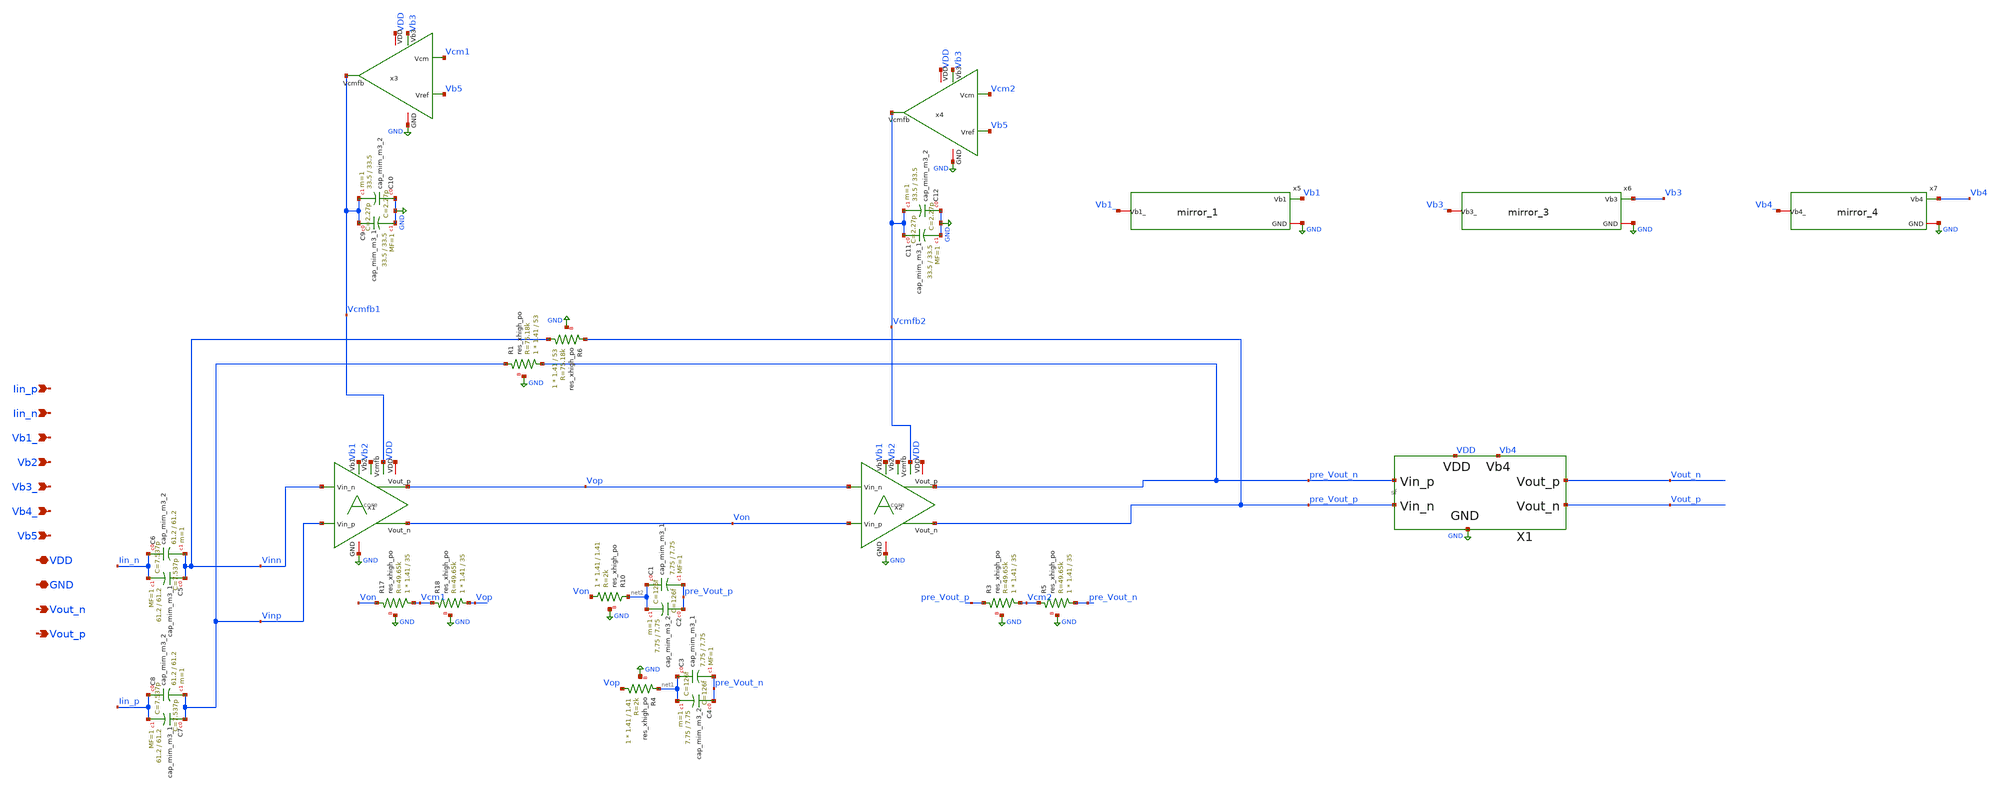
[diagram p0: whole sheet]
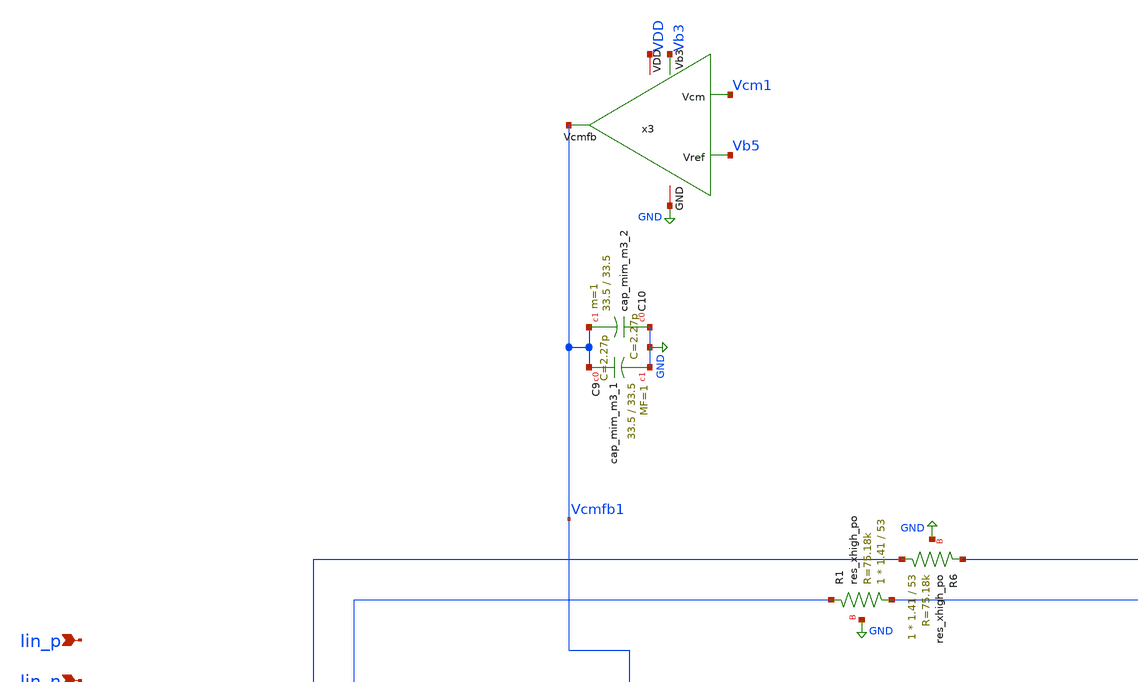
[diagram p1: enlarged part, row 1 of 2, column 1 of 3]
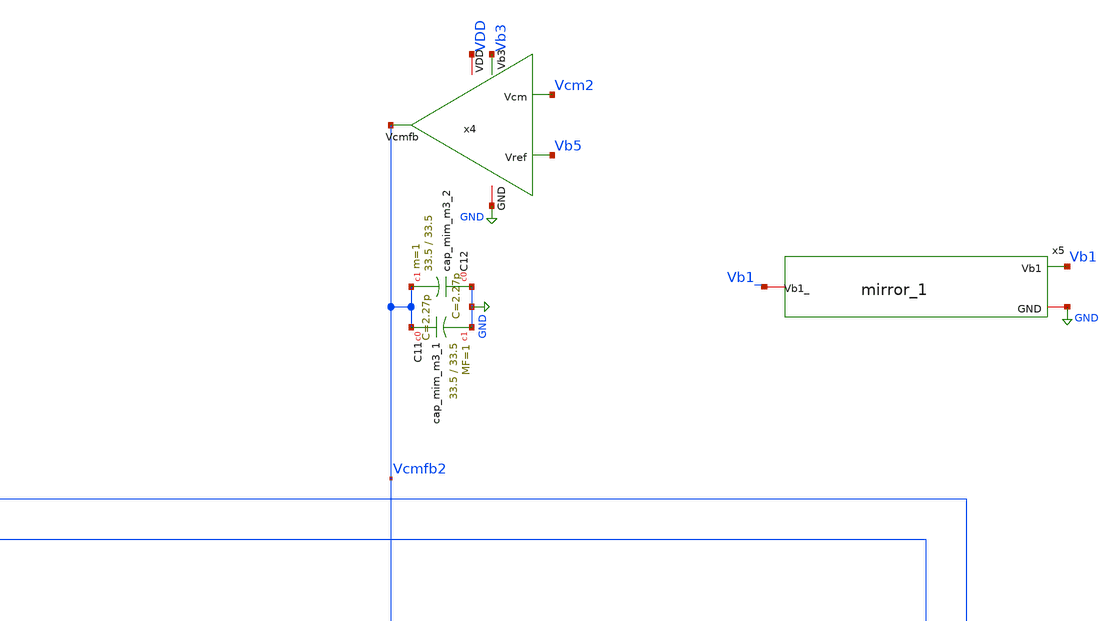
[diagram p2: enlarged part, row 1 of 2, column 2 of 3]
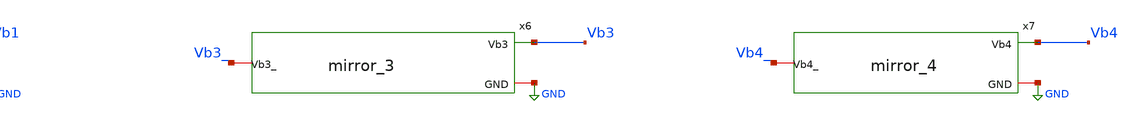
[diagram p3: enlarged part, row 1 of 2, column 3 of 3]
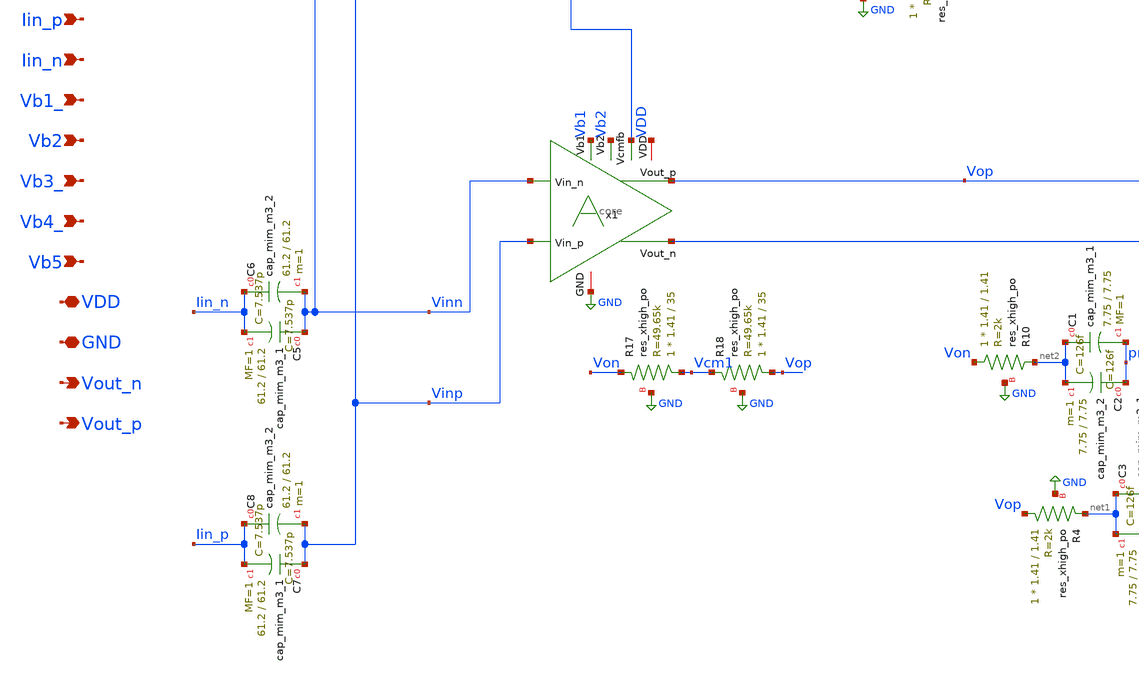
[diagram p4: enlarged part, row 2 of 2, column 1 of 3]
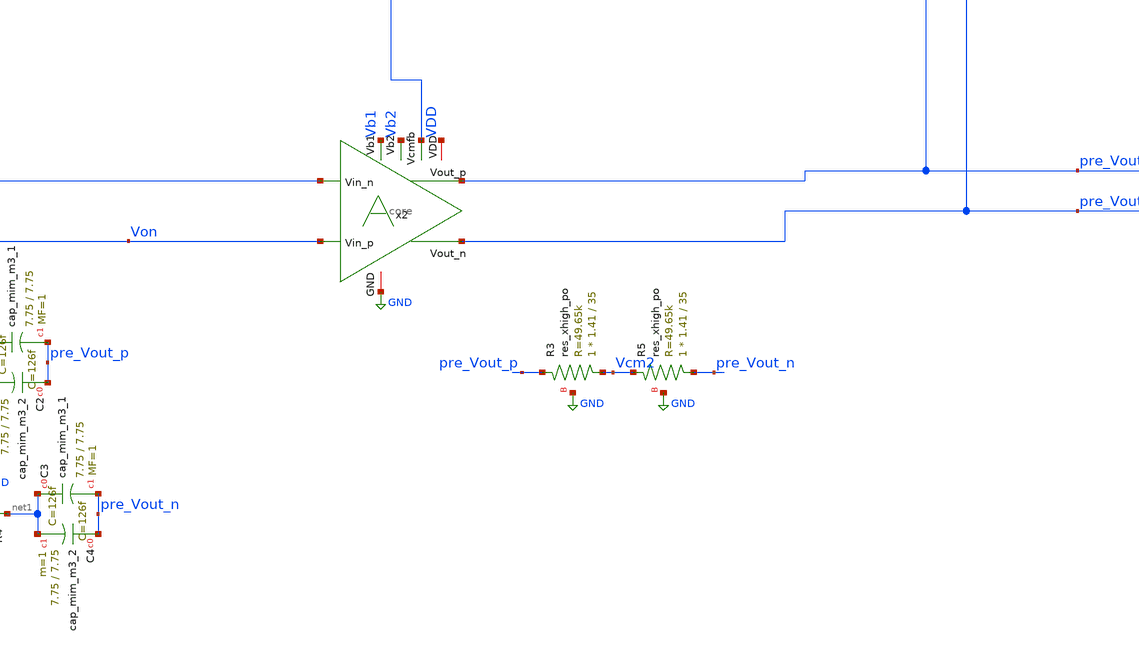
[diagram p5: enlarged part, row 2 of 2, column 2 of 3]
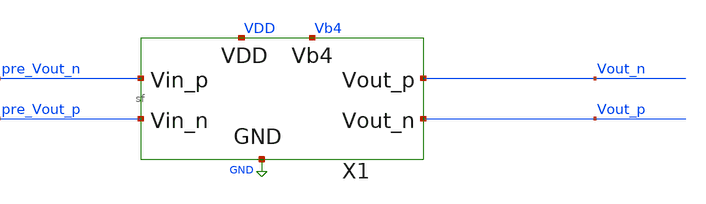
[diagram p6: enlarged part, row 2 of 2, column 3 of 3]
** sch_path: xschem/top.sch
**.subckt top VDD GND Vout_n Iin_n Iin_p Vb1_ Vout_p Vb2 Vb3_ Vb4_ Vb5
*.iopin VDD
*.iopin GND
*.opin Vout_n
*.ipin Iin_n
*.ipin Iin_p
*.ipin Vb1_
*.opin Vout_p
*.ipin Vb2
*.ipin Vb3_
*.ipin Vb4_
*.ipin Vb5
XR6 Vinn pre_Vout_p GND sky130_fd_pr__res_xhigh_po W=1.41 L=53 mult=1 m=1
XR1 pre_Vout_n Vinp GND sky130_fd_pr__res_xhigh_po W=1.41 L=53 mult=1 m=1
XR3 Vcm2 pre_Vout_p GND sky130_fd_pr__res_xhigh_po W=1.41 L=35 mult=1 m=1
XR5 pre_Vout_n Vcm2 GND sky130_fd_pr__res_xhigh_po W=1.41 L=35 mult=1 m=1
XR4 Vop net1 GND sky130_fd_pr__res_xhigh_po W=1.41 L=1.41 mult=1 m=1
XR10 Von net2 GND sky130_fd_pr__res_xhigh_po W=1.41 L=1.41 mult=1 m=1
XR17 Vcm1 Von GND sky130_fd_pr__res_xhigh_po W=1.41 L=35 mult=1 m=1
XR18 Vop Vcm1 GND sky130_fd_pr__res_xhigh_po W=1.41 L=35 mult=1 m=1
x1 Vinn Vinp Vb2 Vb1 Vcmfb1 VDD GND Vop Von core
x2 Vop Von Vb2 Vb1 Vcmfb2 VDD GND pre_Vout_n pre_Vout_p core
X1 VDD GND pre_Vout_n pre_Vout_p Vout_n Vout_p Vb4 sf
x3 Vcm1 Vb5 Vb3 VDD GND Vcmfb1 cmfb
x4 Vcm2 Vb5 Vb3 VDD GND Vcmfb2 cmfb
x5 Vb1 Vb1_ GND mirror_1
x6 Vb3 Vb3_ GND mirror_3
x7 Vb4 Vb4_ GND mirror_4
XC3 net1 pre_Vout_n sky130_fd_pr__cap_mim_m3_1 W=7.75 L=7.75 MF=1 m=1
XC4 pre_Vout_n net1 sky130_fd_pr__cap_mim_m3_2 W=7.75 L=7.75 MF=1 m=1
XC1 net2 pre_Vout_p sky130_fd_pr__cap_mim_m3_1 W=7.75 L=7.75 MF=1 m=1
XC2 pre_Vout_p net2 sky130_fd_pr__cap_mim_m3_2 W=7.75 L=7.75 MF=1 m=1
XC5 Vinn Iin_n sky130_fd_pr__cap_mim_m3_1 W=61.2 L=61.2 MF=1 m=1
XC6 Iin_n Vinn sky130_fd_pr__cap_mim_m3_2 W=61.2 L=61.2 MF=1 m=1
XC7 Vinp Iin_p sky130_fd_pr__cap_mim_m3_1 W=61.2 L=61.2 MF=1 m=1
XC8 Iin_p Vinp sky130_fd_pr__cap_mim_m3_2 W=61.2 L=61.2 MF=1 m=1
XC9 Vcmfb1 GND sky130_fd_pr__cap_mim_m3_1 W=33.5 L=33.5 MF=1 m=1
XC10 GND Vcmfb1 sky130_fd_pr__cap_mim_m3_2 W=33.5 L=33.5 MF=1 m=1
XC11 Vcmfb2 GND sky130_fd_pr__cap_mim_m3_1 W=33.5 L=33.5 MF=1 m=1
XC12 GND Vcmfb2 sky130_fd_pr__cap_mim_m3_2 W=33.5 L=33.5 MF=1 m=1
**.ends

* expanding   symbol:  tia_post_approval/schem/core.sym # of pins=9
** sym_path: tia_post_approval/schem/core.sym
** sch_path: tia_post_approval/schem/core.sch
.subckt core Vin_n Vin_p Vb2 Vb1 Vcmfb VDD GND Vout_p Vout_n
*.ipin Vb2
*.ipin Vcmfb
*.iopin VDD
*.iopin GND
*.opin Vout_p
*.ipin Vin_p
*.ipin Vin_n
*.opin Vout_n
*.ipin Vb1
XM1 net1 Vb1 GND GND sky130_fd_pr__nfet_01v8 L=.5 W=710 nf=8 ad='int((nf+1)/2) * W/nf * 0.29' as='int((nf+2)/2) * W/nf * 0.29'
+ pd='2*int((nf+1)/2) * (W/nf + 0.29)' ps='2*int((nf+2)/2) * (W/nf + 0.29)' nrd='0.29 / W' nrs='0.29 / W'
+ sa=0 sb=0 sd=0 mult=1 m=1
x1 Vin_p Vb2 Vcmfb VDD GND Vout_n net1 core_half
x2 Vin_n Vb2 Vcmfb VDD GND Vout_p net1 core_half
.ends


* expanding   symbol:  tia_post_approval/schem/sf.sym # of pins=7
** sym_path: tia_post_approval/schem/sf.sym
** sch_path: tia_post_approval/schem/sf.sch
.subckt sf VDD GND Vin_p Vin_n Vout_p Vout_n Vb4
*.ipin Vin_n
*.iopin VDD
*.iopin GND
*.ipin Vin_p
*.opin Vout_n
*.opin Vout_p
*.iopin Vb4
X1 VDD Vb4 Vout_p Vin_p GND sf_half
X2 VDD Vb4 Vout_n Vin_n GND sf_half
.ends


* expanding   symbol:  tia_post_approval/schem/cmfb.sym # of pins=6
** sym_path: tia_post_approval/schem/cmfb.sym
** sch_path: tia_post_approval/schem/cmfb.sch
.subckt cmfb Vcm Vref Vb3 VDD GND Vcmfb
*.iopin VDD
*.iopin GND
*.opin Vcmfb
*.ipin Vref
*.iopin Vb3
*.ipin Vcm
x1 Vref net2 VDD GND Vb3 net3 Vcmfb cmfb_half
x2 Vcm net1 VDD GND Vb3 net3 net3 cmfb_half
XR20 net2 net1 GND sky130_fd_pr__res_xhigh_po W=1.41 L=1.41 mult=1 m=1
.ends


* expanding   symbol:  tia_post_approval/schem/mirror_1.sym # of pins=3
** sym_path: tia_post_approval/schem/mirror_1.sym
** sch_path: tia_post_approval/schem/mirror_1.sch
.subckt mirror_1 Vb1 Vb1_ GND
*.iopin GND
*.iopin Vb1_
*.opin Vb1
XM27 Vb1_ Vb1_ GND GND sky130_fd_pr__nfet_01v8 L=.5 W=3.6 nf=1 ad='int((nf+1)/2) * W/nf * 0.29' as='int((nf+2)/2) * W/nf * 0.29'
+ pd='2*int((nf+1)/2) * (W/nf + 0.29)' ps='2*int((nf+2)/2) * (W/nf + 0.29)' nrd='0.29 / W' nrs='0.29 / W'
+ sa=0 sb=0 sd=0 mult=1 m=1
XC1 Vb1 GND sky130_fd_pr__cap_mim_m3_1 W=15.8 L=15.8 MF=1 m=1
XC2 GND Vb1 sky130_fd_pr__cap_mim_m3_2 W=15.8 L=15.8 MF=1 m=1
XR11 V10 Vb1 GND sky130_fd_pr__res_xhigh_po W=0.35 L=16 mult=1 m=1
XR1 Vb1_ V1 GND sky130_fd_pr__res_xhigh_po W=0.35 L=16 mult=1 m=1
XR2 V10 V9 GND sky130_fd_pr__res_xhigh_po W=0.35 L=16 mult=1 m=1
XR3 V2 V1 GND sky130_fd_pr__res_xhigh_po W=0.35 L=16 mult=1 m=1
XR4 V8 V9 GND sky130_fd_pr__res_xhigh_po W=0.35 L=16 mult=1 m=1
XR5 V2 V3 GND sky130_fd_pr__res_xhigh_po W=0.35 L=16 mult=1 m=1
XR6 V8 V7 GND sky130_fd_pr__res_xhigh_po W=0.35 L=16 mult=1 m=1
XR7 V4 V3 GND sky130_fd_pr__res_xhigh_po W=0.35 L=16 mult=1 m=1
XR8 V6 V7 GND sky130_fd_pr__res_xhigh_po W=0.35 L=16 mult=1 m=1
XR9 V4 V5 GND sky130_fd_pr__res_xhigh_po W=0.35 L=16 mult=1 m=1
XR10 V6 V5 GND sky130_fd_pr__res_xhigh_po W=0.35 L=16 mult=1 m=1
XM1 GND GND Vb1_ GND sky130_fd_pr__nfet_01v8 L=.5 W=3.6 nf=1 ad='int((nf+1)/2) * W/nf * 0.29' as='int((nf+2)/2) * W/nf * 0.29'
+ pd='2*int((nf+1)/2) * (W/nf + 0.29)' ps='2*int((nf+2)/2) * (W/nf + 0.29)' nrd='0.29 / W' nrs='0.29 / W'
+ sa=0 sb=0 sd=0 mult=1 m=1
XM2 GND GND GND GND sky130_fd_pr__nfet_01v8 L=.5 W=3.6 nf=1 ad='int((nf+1)/2) * W/nf * 0.29' as='int((nf+2)/2) * W/nf * 0.29'
+ pd='2*int((nf+1)/2) * (W/nf + 0.29)' ps='2*int((nf+2)/2) * (W/nf + 0.29)' nrd='0.29 / W' nrs='0.29 / W'
+ sa=0 sb=0 sd=0 mult=1 m=1
.ends


* expanding   symbol:  tia_post_approval/schem/mirror_3.sym # of pins=3
** sym_path: tia_post_approval/schem/mirror_3.sym
** sch_path: tia_post_approval/schem/mirror_3.sch
.subckt mirror_3 Vb3 Vb3_ GND
*.iopin GND
*.iopin Vb3_
*.opin Vb3
XM27 Vb3_ Vb3_ GND GND sky130_fd_pr__nfet_01v8 L=.5 W=5 nf=1 ad='int((nf+1)/2) * W/nf * 0.29' as='int((nf+2)/2) * W/nf * 0.29'
+ pd='2*int((nf+1)/2) * (W/nf + 0.29)' ps='2*int((nf+2)/2) * (W/nf + 0.29)' nrd='0.29 / W' nrs='0.29 / W'
+ sa=0 sb=0 sd=0 mult=2 m=2
XR11 V10 Vb3 GND sky130_fd_pr__res_xhigh_po W=0.35 L=16 mult=1 m=1
XC1 Vb3 GND sky130_fd_pr__cap_mim_m3_1 W=15.8 L=15.8 MF=1 m=1
XC2 GND Vb3 sky130_fd_pr__cap_mim_m3_2 W=15.8 L=15.8 MF=1 m=1
XR1 Vb3_ V1 GND sky130_fd_pr__res_xhigh_po W=0.35 L=16 mult=1 m=1
XR2 V10 V9 GND sky130_fd_pr__res_xhigh_po W=0.35 L=16 mult=1 m=1
XR3 V2 V1 GND sky130_fd_pr__res_xhigh_po W=0.35 L=16 mult=1 m=1
XR4 V8 V9 GND sky130_fd_pr__res_xhigh_po W=0.35 L=16 mult=1 m=1
XR5 V2 V3 GND sky130_fd_pr__res_xhigh_po W=0.35 L=16 mult=1 m=1
XR6 V8 V7 GND sky130_fd_pr__res_xhigh_po W=0.35 L=16 mult=1 m=1
XR7 V4 V3 GND sky130_fd_pr__res_xhigh_po W=0.35 L=16 mult=1 m=1
XR8 V6 V7 GND sky130_fd_pr__res_xhigh_po W=0.35 L=16 mult=1 m=1
XR9 V4 V5 GND sky130_fd_pr__res_xhigh_po W=0.35 L=16 mult=1 m=1
XR10 V6 V5 GND sky130_fd_pr__res_xhigh_po W=0.35 L=16 mult=1 m=1
.ends


* expanding   symbol:  tia_post_approval/schem/mirror_4.sym # of pins=3
** sym_path: tia_post_approval/schem/mirror_4.sym
** sch_path: tia_post_approval/schem/mirror_4.sch
.subckt mirror_4 Vb4 Vb4_ GND
*.iopin GND
*.iopin Vb4_
*.opin Vb4
XM27 Vb4_ Vb4_ GND GND sky130_fd_pr__nfet_01v8 L=.45 W=4 nf=1 ad='int((nf+1)/2) * W/nf * 0.29' as='int((nf+2)/2) * W/nf * 0.29'
+ pd='2*int((nf+1)/2) * (W/nf + 0.29)' ps='2*int((nf+2)/2) * (W/nf + 0.29)' nrd='0.29 / W' nrs='0.29 / W'
+ sa=0 sb=0 sd=0 mult=1 m=1
XC1 Vb4 GND sky130_fd_pr__cap_mim_m3_1 W=15.8 L=15.8 MF=1 m=1
XC2 GND Vb4 sky130_fd_pr__cap_mim_m3_2 W=15.8 L=15.8 MF=1 m=1
XR11 V10 Vb4 GND sky130_fd_pr__res_xhigh_po W=0.35 L=16 mult=1 m=1
XR1 Vb4_ V1 GND sky130_fd_pr__res_xhigh_po W=0.35 L=16 mult=1 m=1
XR2 V10 V9 GND sky130_fd_pr__res_xhigh_po W=0.35 L=16 mult=1 m=1
XR3 V2 V1 GND sky130_fd_pr__res_xhigh_po W=0.35 L=16 mult=1 m=1
XR4 V8 V9 GND sky130_fd_pr__res_xhigh_po W=0.35 L=16 mult=1 m=1
XR5 V2 V3 GND sky130_fd_pr__res_xhigh_po W=0.35 L=16 mult=1 m=1
XR6 V8 V7 GND sky130_fd_pr__res_xhigh_po W=0.35 L=16 mult=1 m=1
XR7 V4 V3 GND sky130_fd_pr__res_xhigh_po W=0.35 L=16 mult=1 m=1
XR8 V6 V7 GND sky130_fd_pr__res_xhigh_po W=0.35 L=16 mult=1 m=1
XR9 V4 V5 GND sky130_fd_pr__res_xhigh_po W=0.35 L=16 mult=1 m=1
XR10 V6 V5 GND sky130_fd_pr__res_xhigh_po W=0.35 L=16 mult=1 m=1
.ends


* expanding   symbol:  tia_post_approval/schem/core_half.sym # of pins=7
** sym_path: tia_post_approval/schem/core_half.sym
** sch_path: tia_post_approval/schem/core_half.sch
.subckt core_half Vin Vb2 Vcmfb VDD GND Vout s
*.ipin Vb2
*.ipin Vcmfb
*.iopin VDD
*.iopin GND
*.opin Vout
*.iopin s
*.ipin Vin
XM3 Vout Vin s GND sky130_fd_pr__nfet_01v8 L=0.15 W=150 nf=4 ad='int((nf+1)/2) * W/nf * 0.29' as='int((nf+2)/2) * W/nf * 0.29'
+ pd='2*int((nf+1)/2) * (W/nf + 0.29)' ps='2*int((nf+2)/2) * (W/nf + 0.29)' nrd='0.29 / W' nrs='0.29 / W'
+ sa=0 sb=0 sd=0 mult=1 m=1
XM5 Vout Vcmfb VDD VDD sky130_fd_pr__pfet_01v8 L=0.18 W=112 nf=5 ad='int((nf+1)/2) * W/nf * 0.29' as='int((nf+2)/2) * W/nf * 0.29'
+ pd='2*int((nf+1)/2) * (W/nf + 0.29)' ps='2*int((nf+2)/2) * (W/nf + 0.29)' nrd='0.29 / W' nrs='0.29 / W'
+ sa=0 sb=0 sd=0 mult=1 m=1
XM25 Vout Vb2 VDD VDD sky130_fd_pr__pfet_01v8 L=0.18 W=448 nf=15 ad='int((nf+1)/2) * W/nf * 0.29' as='int((nf+2)/2) * W/nf * 0.29'
+ pd='2*int((nf+1)/2) * (W/nf + 0.29)' ps='2*int((nf+2)/2) * (W/nf + 0.29)' nrd='0.29 / W' nrs='0.29 / W'
+ sa=0 sb=0 sd=0 mult=1 m=1
.ends


* expanding   symbol:  tia_post_approval/schem/sf_half.sym # of pins=5
** sym_path: tia_post_approval/schem/sf_half.sym
** sch_path: tia_post_approval/schem/sf_half.sch
.subckt sf_half VDD g_d Vout g_u GND
*.iopin VDD
*.iopin g_u
*.iopin GND
*.iopin Vout
*.iopin g_d
XM17 VDD g_u Vout GND sky130_fd_pr__nfet_01v8_lvt L=0.32 W=650 nf=26 ad='int((nf+1)/2) * W/nf * 0.29'
+ as='int((nf+2)/2) * W/nf * 0.29' pd='2*int((nf+1)/2) * (W/nf + 0.29)' ps='2*int((nf+2)/2) * (W/nf + 0.29)'
+ nrd='0.29 / W' nrs='0.29 / W' sa=0 sb=0 sd=0 mult=1 m=1
XM19 Vout g_d GND GND sky130_fd_pr__nfet_01v8 L=.45 W=650 nf=26 ad='int((nf+1)/2) * W/nf * 0.29' as='int((nf+2)/2) * W/nf * 0.29'
+ pd='2*int((nf+1)/2) * (W/nf + 0.29)' ps='2*int((nf+2)/2) * (W/nf + 0.29)' nrd='0.29 / W' nrs='0.29 / W'
+ sa=0 sb=0 sd=0 mult=1 m=1
.ends


* expanding   symbol:  tia_post_approval/schem/cmfb_half.sym # of pins=7
** sym_path: tia_post_approval/schem/cmfb_half.sym
** sch_path: tia_post_approval/schem/cmfb_half.sch
.subckt cmfb_half Vin res VDD GND Vb3 diode Vout
*.iopin VDD
*.iopin GND
*.opin Vout
*.ipin Vin
*.iopin diode
*.iopin Vb3
*.iopin res
XM11 Vout Vin res GND sky130_fd_pr__nfet_01v8 L=0.20 W=150 nf=2 ad='int((nf+1)/2) * W/nf * 0.29' as='int((nf+2)/2) * W/nf * 0.29'
+ pd='2*int((nf+1)/2) * (W/nf + 0.29)' ps='2*int((nf+2)/2) * (W/nf + 0.29)' nrd='0.29 / W' nrs='0.29 / W'
+ sa=0 sb=0 sd=0 mult=1 m=1
XM14 Vout diode VDD VDD sky130_fd_pr__pfet_01v8 L=0.2 W=42 nf=1 ad='int((nf+1)/2) * W/nf * 0.29' as='int((nf+2)/2) * W/nf * 0.29'
+ pd='2*int((nf+1)/2) * (W/nf + 0.29)' ps='2*int((nf+2)/2) * (W/nf + 0.29)' nrd='0.29 / W' nrs='0.29 / W'
+ sa=0 sb=0 sd=0 mult=1 m=1
XM15 res Vb3 GND GND sky130_fd_pr__nfet_01v8 L=.5 W=65 nf=1 ad='int((nf+1)/2) * W/nf * 0.29' as='int((nf+2)/2) * W/nf * 0.29'
+ pd='2*int((nf+1)/2) * (W/nf + 0.29)' ps='2*int((nf+2)/2) * (W/nf + 0.29)' nrd='0.29 / W' nrs='0.29 / W'
+ sa=0 sb=0 sd=0 mult=1 m=1
.ends

.GLOBAL GND
.end
